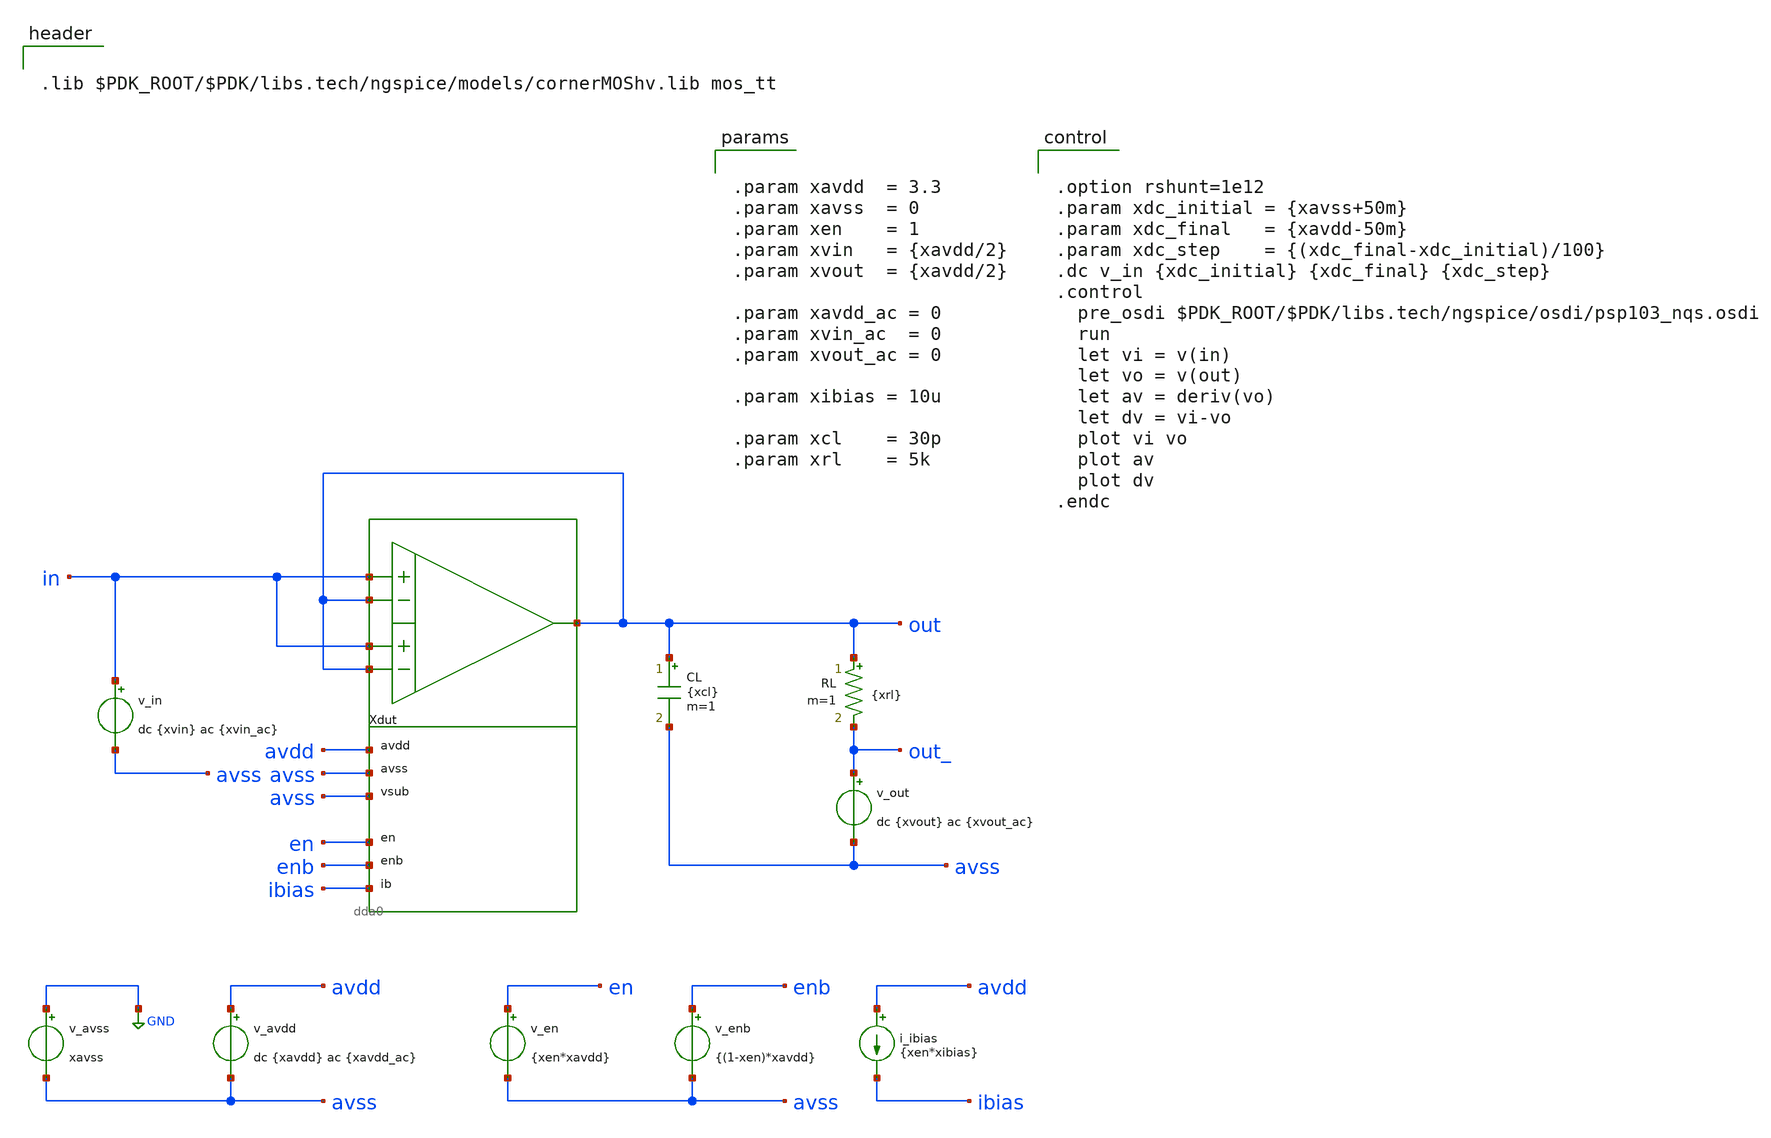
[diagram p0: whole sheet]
** sch_path: xschem/tb_dda0_buf_dc.sch
**.subckt tb_dda0_buf_dc
Xdut in out in out out avdd avss avss en enb ibias dda0
v_avss GND avss xavss
v_avdd avdd avss dc {xavdd} ac {xavdd_ac}
v_in in avss dc {xvin} ac {xvin_ac}
v_en en avss {xen*xavdd}
v_enb enb avss {(1-xen)*xavdd}
i_ibias avdd ibias {xen*xibias}
CL out avss {xcl} m=1
v_out out_ avss dc {xvout} ac {xvout_ac}
RL out out_ {xrl} m=1
**** begin user architecture code


.lib $PDK_ROOT/$PDK/libs.tech/ngspice/models/cornerMOShv.lib mos_tt




.option rshunt=1e12
.param xdc_initial = {xavss+50m}
.param xdc_final   = {xavdd-50m}
.param xdc_step    = {(xdc_final-xdc_initial)/100}
.dc v_in {xdc_initial} {xdc_final} {xdc_step}
.control
  pre_osdi $PDK_ROOT/$PDK/libs.tech/ngspice/osdi/psp103_nqs.osdi
  run
  let vi = v(in)
  let vo = v(out)
  let av = deriv(vo)
  let dv = vi-vo
  plot vi vo
  plot av
  plot dv
.endc




.param xavdd  = 3.3
.param xavss  = 0
.param xen    = 1
.param xvin   = {xavdd/2}
.param xvout  = {xavdd/2}

.param xavdd_ac = 0
.param xvin_ac  = 0
.param xvout_ac = 0

.param xibias = 10u

.param xcl    = 30p
.param xrl    = 5k


**** end user architecture code
**.ends
.GLOBAL GND
.end
